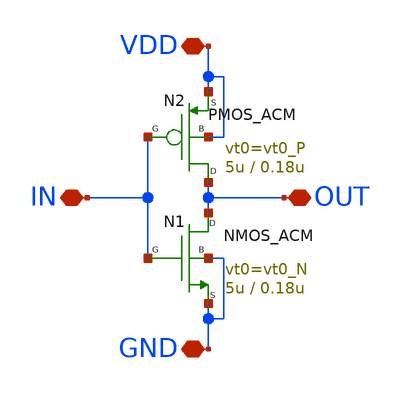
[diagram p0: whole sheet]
** sch_path: gf_tutorials/ACM/inverter_acm.sch
**.subckt inverter_acm IN VDD GND OUT
*.iopin IN
*.iopin VDD
*.iopin GND
*.iopin OUT
N1 OUT IN GND GND NMOS_ACM w=5u l=0.18u n=1.37 is=5.52u vt0=vt0_N sigma=27m zeta=56m
N2 OUT IN VDD VDD PMOS_ACM w=5u l=0.18u n=1.40 is=1.82u vt0=vt0_P sigma=24m zeta=35m
**.ends
.end
